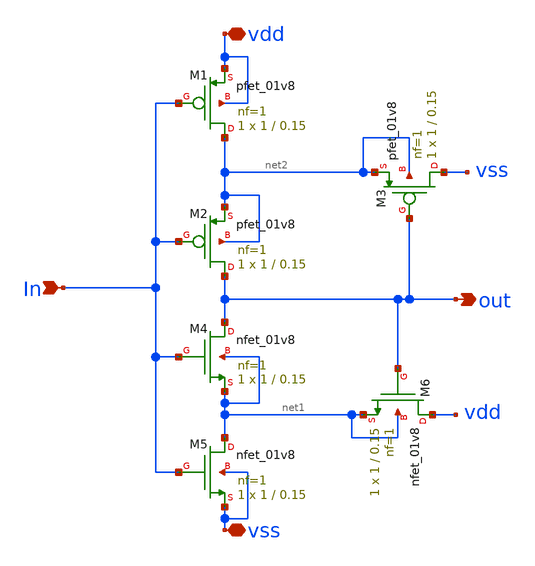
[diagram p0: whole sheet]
** sch_path: Component_Library/ST_INVERTER/schematic/ST_INVERTER.sch
**.subckt ST_INVERTER In out vdd vss
*.ipin In
*.opin out
*.iopin vdd
*.iopin vss
XM2 out In net2 net2 sky130_fd_pr__pfet_01v8 L=0.15 W=1 nf=1 ad='int((nf+1)/2) * W/nf * 0.29' as='int((nf+2)/2) * W/nf * 0.29'
+ pd='2*int((nf+1)/2) * (W/nf + 0.29)' ps='2*int((nf+2)/2) * (W/nf + 0.29)' nrd='0.29 / W' nrs='0.29 / W'
+ sa=0 sb=0 sd=0 mult=1 m=1
XM3 vss out net2 net2 sky130_fd_pr__pfet_01v8 L=0.15 W=1 nf=1 ad='int((nf+1)/2) * W/nf * 0.29' as='int((nf+2)/2) * W/nf * 0.29'
+ pd='2*int((nf+1)/2) * (W/nf + 0.29)' ps='2*int((nf+2)/2) * (W/nf + 0.29)' nrd='0.29 / W' nrs='0.29 / W'
+ sa=0 sb=0 sd=0 mult=1 m=1
XM1 net2 In vdd vdd sky130_fd_pr__pfet_01v8 L=0.15 W=1 nf=1 ad='int((nf+1)/2) * W/nf * 0.29' as='int((nf+2)/2) * W/nf * 0.29'
+ pd='2*int((nf+1)/2) * (W/nf + 0.29)' ps='2*int((nf+2)/2) * (W/nf + 0.29)' nrd='0.29 / W' nrs='0.29 / W'
+ sa=0 sb=0 sd=0 mult=1 m=1
XM4 out In net1 net1 sky130_fd_pr__nfet_01v8 L=0.15 W=1 nf=1 ad='int((nf+1)/2) * W/nf * 0.29' as='int((nf+2)/2) * W/nf * 0.29'
+ pd='2*int((nf+1)/2) * (W/nf + 0.29)' ps='2*int((nf+2)/2) * (W/nf + 0.29)' nrd='0.29 / W' nrs='0.29 / W'
+ sa=0 sb=0 sd=0 mult=1 m=1
XM5 net1 In vss vss sky130_fd_pr__nfet_01v8 L=0.15 W=1 nf=1 ad='int((nf+1)/2) * W/nf * 0.29' as='int((nf+2)/2) * W/nf * 0.29'
+ pd='2*int((nf+1)/2) * (W/nf + 0.29)' ps='2*int((nf+2)/2) * (W/nf + 0.29)' nrd='0.29 / W' nrs='0.29 / W'
+ sa=0 sb=0 sd=0 mult=1 m=1
XM6 vdd out net1 net1 sky130_fd_pr__nfet_01v8 L=0.15 W=1 nf=1 ad='int((nf+1)/2) * W/nf * 0.29' as='int((nf+2)/2) * W/nf * 0.29'
+ pd='2*int((nf+1)/2) * (W/nf + 0.29)' ps='2*int((nf+2)/2) * (W/nf + 0.29)' nrd='0.29 / W' nrs='0.29 / W'
+ sa=0 sb=0 sd=0 mult=1 m=1
**.ends
.end
